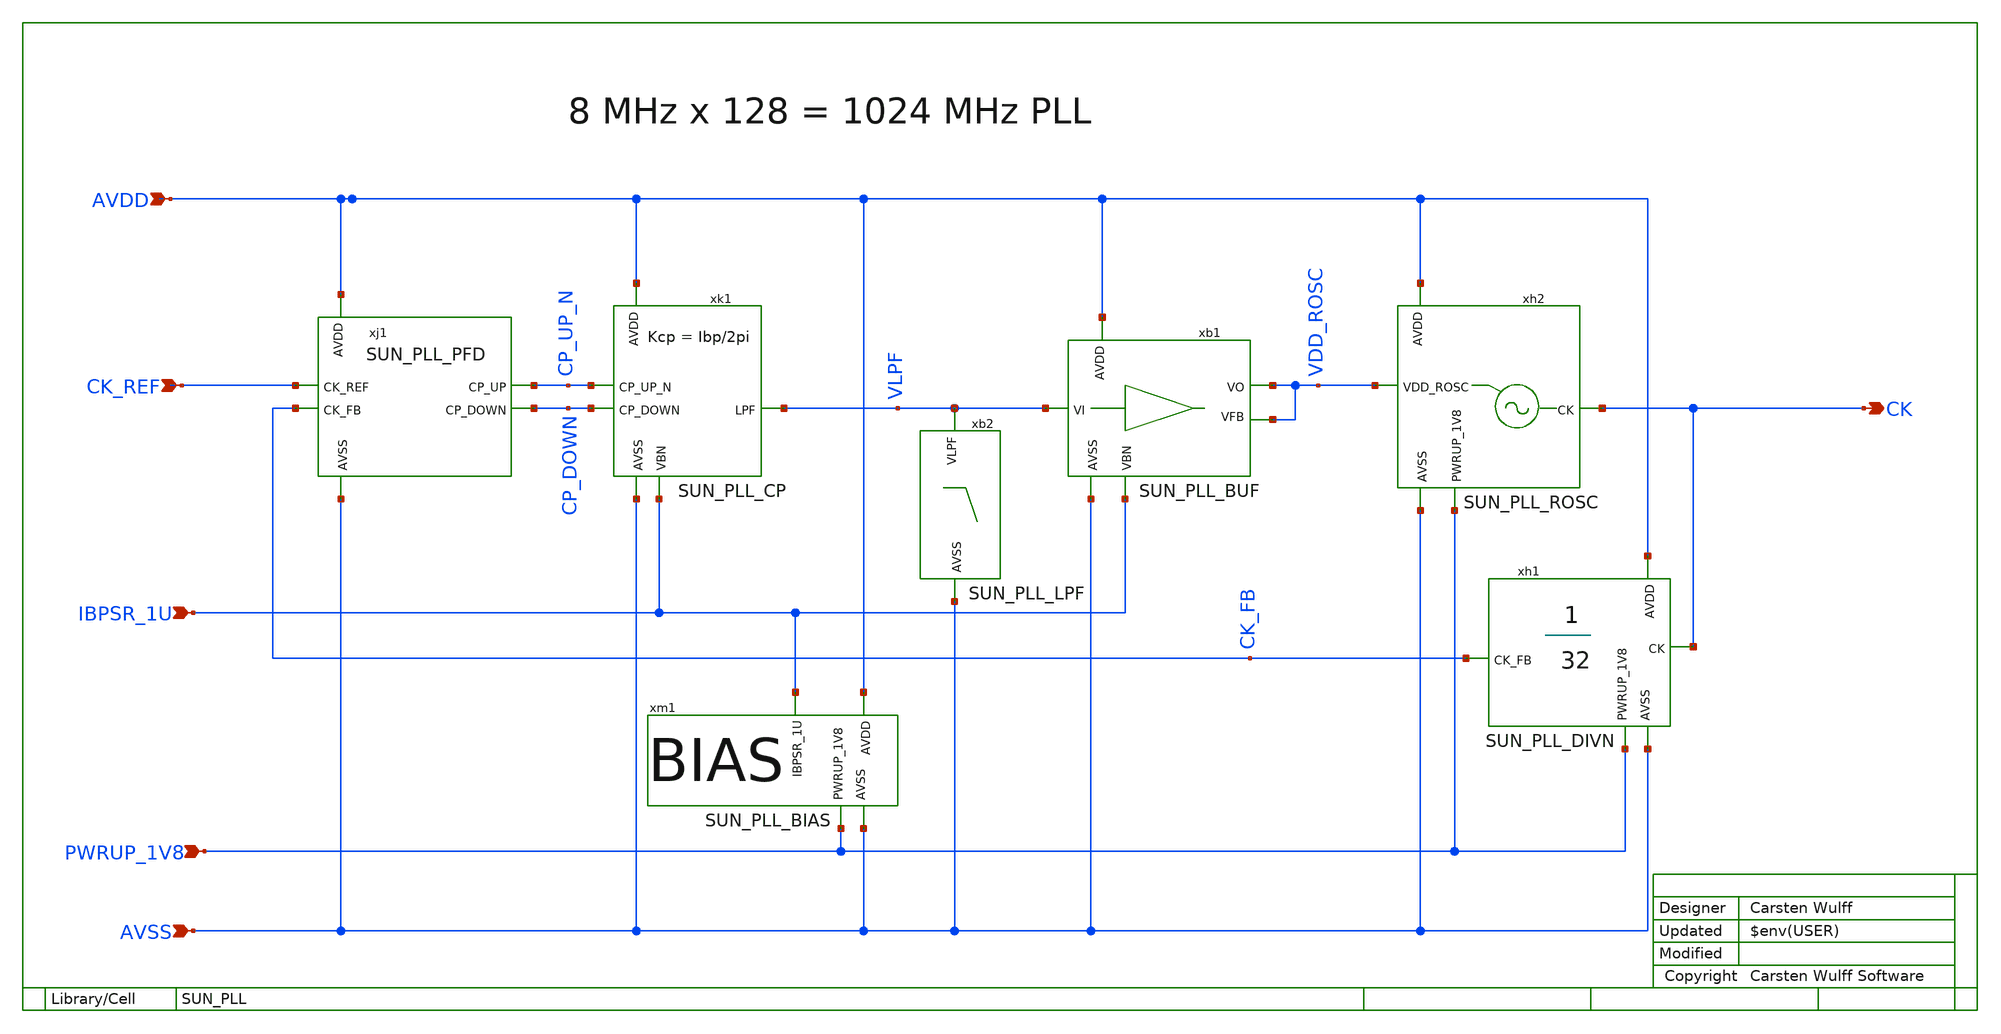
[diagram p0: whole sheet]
** sch_path: ip/sun_pll_sky130nm/design/SUN_PLL_SKY130NM/SUN_PLL.sch
**.subckt SUN_PLL AVDD AVSS PWRUP_1V8 CK_REF CK IBPSR_1U
*.ipin AVDD
*.ipin AVSS
*.ipin PWRUP_1V8
*.ipin CK_REF
*.opin CK
*.ipin IBPSR_1U
xh2 AVDD CK VDD_ROSC PWRUP_1V8 AVSS SUN_PLL_ROSC xoffset=0 yoffset=0 angle=0
xh1 AVDD CK_FB CK PWRUP_1V8 AVSS SUN_PLL_DIVN xoffset=-280 yoffset=12 angle=0
xm1 IBPSR_1U AVDD PWRUP_1V8 AVSS SUN_PLL_BIAS xoffset=70 yoffset=0 angle=0
xb1 AVDD VDD_ROSC VLPF VDD_ROSC IBPSR_1U AVSS SUN_PLL_BUF xoffset=5 yoffset=2 angle=0
xb2 VLPF AVSS SUN_PLL_LPF xoffset=0 yoffset=40 angle=0
xk1 AVDD CP_UP_N VLPF CP_DOWN IBPSR_1U AVSS SUN_PLL_CP xoffset=10 yoffset=107 angle=0
xj1 AVDD CP_UP_N CK_REF CP_DOWN CK_FB AVSS SUN_PLL_PFD
**.ends
.end
